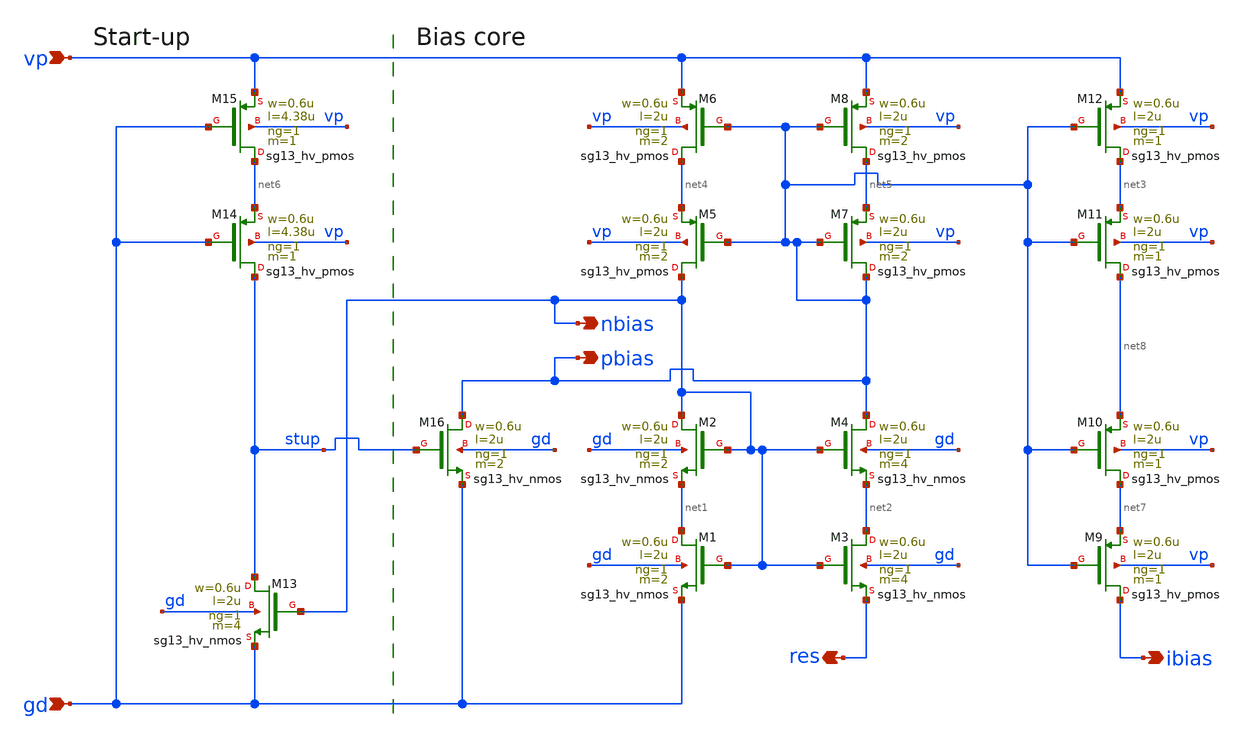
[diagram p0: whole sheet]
** sch_path: circuit/const_gm_bias_core.sch
**.subckt const_gm_bias_core vp gd ibias res nbias pbias
*.ipin vp
*.ipin gd
*.opin ibias
*.opin res
*.opin nbias
*.opin pbias
XM1 net1 nbias gd gd sg13_hv_nmos w=0.6u l=2u ng=1 m=2 mm_ok=1
XM3 net2 nbias res gd sg13_hv_nmos w=0.6u l=2u ng=1 m=4 mm_ok=1
XM8 net5 pbias vp vp sg13_hv_pmos w=0.6u l=2u ng=1 m=2 mm_ok=1
XM6 net4 pbias vp vp sg13_hv_pmos w=0.6u l=2u ng=1 m=2 mm_ok=1
XM12 net3 pbias vp vp sg13_hv_pmos w=0.6u l=2u ng=1 m=1 mm_ok=1
XM15 net6 gd vp vp sg13_hv_pmos w=0.6u l=4.38u ng=1 m=1 mm_ok=1
XM13 stup nbias gd gd sg13_hv_nmos w=0.6u l=2u ng=1 m=4 mm_ok=1
XM16 pbias stup gd gd sg13_hv_nmos w=0.6u l=2u ng=1 m=2 mm_ok=1
XM2 nbias nbias net1 gd sg13_hv_nmos w=0.6u l=2u ng=1 m=2 mm_ok=1
XM4 pbias nbias net2 gd sg13_hv_nmos w=0.6u l=2u ng=1 m=4 mm_ok=1
XM11 net8 pbias net3 vp sg13_hv_pmos w=0.6u l=2u ng=1 m=1 mm_ok=1
XM7 pbias pbias net5 vp sg13_hv_pmos w=0.6u l=2u ng=1 m=2 mm_ok=1
XM5 nbias pbias net4 vp sg13_hv_pmos w=0.6u l=2u ng=1 m=2 mm_ok=1
XM14 stup gd net6 vp sg13_hv_pmos w=0.6u l=4.38u ng=1 m=1 mm_ok=1
XM10 net7 pbias net8 vp sg13_hv_pmos w=0.6u l=2u ng=1 m=1 mm_ok=1
XM9 ibias pbias net7 vp sg13_hv_pmos w=0.6u l=2u ng=1 m=1 mm_ok=1
**.ends
.end
